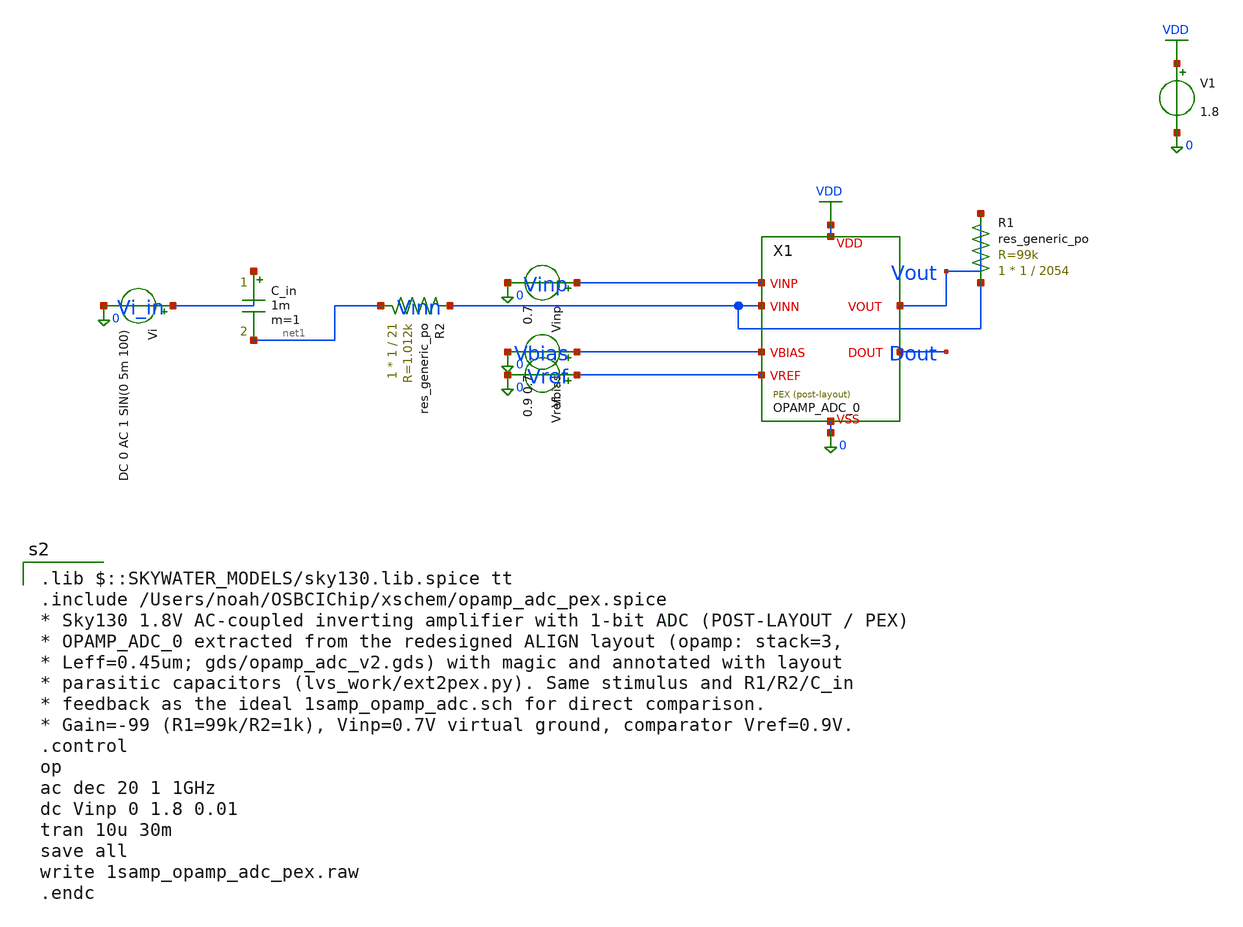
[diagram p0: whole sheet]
** sch_path: first_tapeout_eeg/source/trials/20260902/pex_opamp_adc/xschem/1samp_opamp_adc_pex.sch
**.subckt 1samp_opamp_adc_pex
X1 VDD 0 Vinp Vinn Vbias Vref Vout Dout OPAMP_ADC_0
V1 VDD 0 1.8
Vinp Vinp 0 0.7
Vbias Vbias 0 0.7
Vref Vref 0 0.9
Vi Vi_in 0 DC 0 AC 1 SIN(0 5m 100)
C_in Vi_in net1 1m m=1
XR2 net1 Vinn sky130_fd_pr__res_generic_po W=1 L=21 m=1
XR1 Vinn Vout sky130_fd_pr__res_generic_po W=1 L=2054 m=1
**** begin user architecture code
 .lib $::SKYWATER_MODELS/sky130.lib.spice tt
.include /Users/noah/OSBCIChip/xschem/opamp_adc_pex.spice
* Sky130 1.8V AC-coupled inverting amplifier with 1-bit ADC (POST-LAYOUT / PEX)
* OPAMP_ADC_0 extracted from the redesigned ALIGN layout (opamp: stack=3,
* Leff=0.45um; gds/opamp_adc_v2.gds) with magic and annotated with layout
* parasitic capacitors (lvs_work/ext2pex.py). Same stimulus and R1/R2/C_in
* feedback as the ideal 1samp_opamp_adc.sch for direct comparison.
* Gain=-99 (R1=99k/R2=1k), Vinp=0.7V virtual ground, comparator Vref=0.9V.
.control
op
ac dec 20 1 1GHz
dc Vinp 0 1.8 0.01
tran 10u 30m
save all
write 1samp_opamp_adc_pex.raw
.endc
**** end user architecture code
**.ends
.GLOBAL VDD
.end
